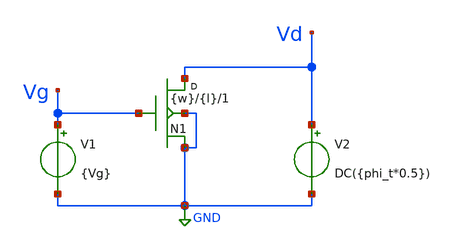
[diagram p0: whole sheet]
** sch_path: Parametros_Vaf/VTH_tets.sch
**.subckt VTH_tets
N1 Vd Vg GND GND NMOS_ACM w={w} l={l} m=1
V1 Vg GND {Vg}
V2 Vd GND DC({phi_t*0.5})
**** begin user architecture code


* Circuit Parameters
.param vg = 3
.param step = 0.01
.param phi_t = 0.0258
.param w = 5.0u
.param l = 0.18u
* Include Models
.model NMOS_ACM nmos_ACM
.model PMOS_ACM pmos_ACM
* OP Parameters & Singals to save
.save all
.save @n1[gm_op]
*Simulations
.dc V1 0 {vg} {step}
.control
pre_osdi NMOS_ACM_2V0.osdi
pre_osdi PMOS_ACM_2V0.osdi
run
let gm_id = deriv(-1*i(V2))/(-1*i(V2))
setplot dc1
plot gm_id
set filetype = ascii
write dcsweep.raw
.endc
.end


**** end user architecture code
**.ends
.GLOBAL GND
.end
